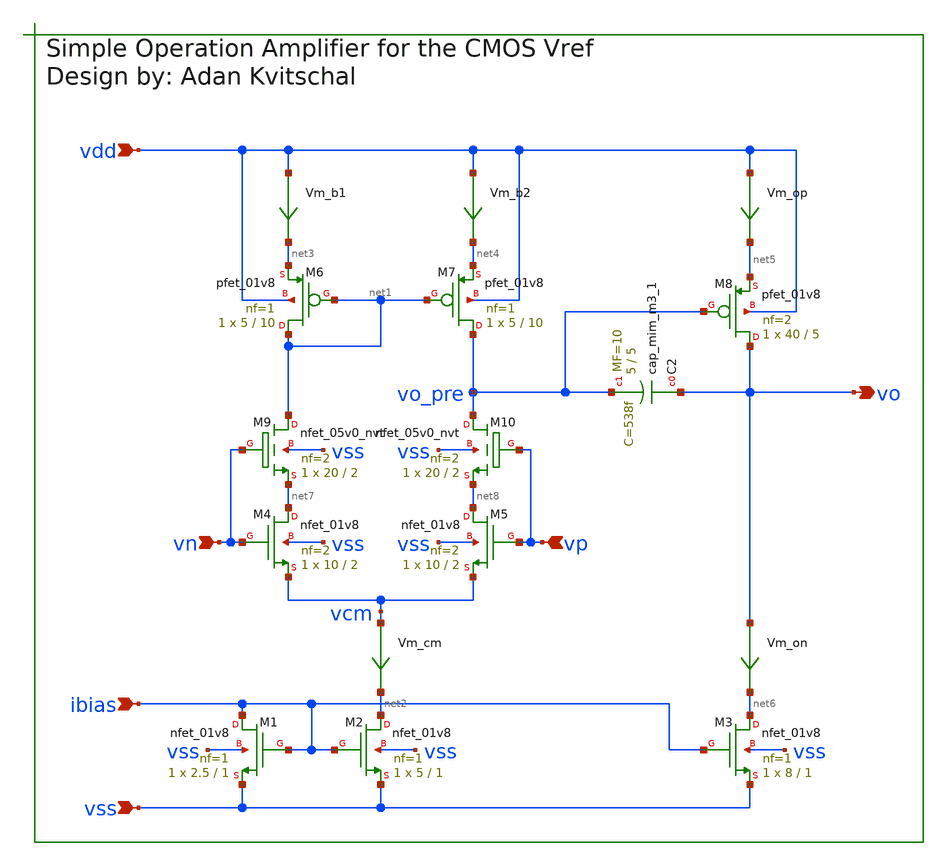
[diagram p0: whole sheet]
** sch_path: xschem/output_amp.sch
**.subckt output_amp vp vn ibias vo vss vdd
*.ipin vp
*.ipin vn
*.ipin ibias
*.opin vo
*.ipin vss
*.ipin vdd
XM1 ibias ibias vss vss sky130_fd_pr__nfet_01v8 L=1 W=2.5 nf=1 ad='int((nf+1)/2) * W/nf * 0.29' as='int((nf+2)/2) * W/nf * 0.29'
+ pd='2*int((nf+1)/2) * (W/nf + 0.29)' ps='2*int((nf+2)/2) * (W/nf + 0.29)' nrd='0.29 / W' nrs='0.29 / W'
+ sa=0 sb=0 sd=0 mult=1 m=1
XM2 net2 ibias vss vss sky130_fd_pr__nfet_01v8 L=1 W=5 nf=1 ad='int((nf+1)/2) * W/nf * 0.29' as='int((nf+2)/2) * W/nf * 0.29'
+ pd='2*int((nf+1)/2) * (W/nf + 0.29)' ps='2*int((nf+2)/2) * (W/nf + 0.29)' nrd='0.29 / W' nrs='0.29 / W'
+ sa=0 sb=0 sd=0 mult=1 m=1
XM7 vo_pre net1 net4 vdd sky130_fd_pr__pfet_01v8 L=10 W=5 nf=1 ad='int((nf+1)/2) * W/nf * 0.29' as='int((nf+2)/2) * W/nf * 0.29'
+ pd='2*int((nf+1)/2) * (W/nf + 0.29)' ps='2*int((nf+2)/2) * (W/nf + 0.29)' nrd='0.29 / W' nrs='0.29 / W'
+ sa=0 sb=0 sd=0 mult=1 m=1
XM4 net7 vn vcm vss sky130_fd_pr__nfet_01v8 L=2 W=10 nf=2 ad='int((nf+1)/2) * W/nf * 0.29' as='int((nf+2)/2) * W/nf * 0.29'
+ pd='2*int((nf+1)/2) * (W/nf + 0.29)' ps='2*int((nf+2)/2) * (W/nf + 0.29)' nrd='0.29 / W' nrs='0.29 / W'
+ sa=0 sb=0 sd=0 mult=1 m=1
XM5 net8 vp vcm vss sky130_fd_pr__nfet_01v8 L=2 W=10 nf=2 ad='int((nf+1)/2) * W/nf * 0.29' as='int((nf+2)/2) * W/nf * 0.29'
+ pd='2*int((nf+1)/2) * (W/nf + 0.29)' ps='2*int((nf+2)/2) * (W/nf + 0.29)' nrd='0.29 / W' nrs='0.29 / W'
+ sa=0 sb=0 sd=0 mult=1 m=1
XM6 net1 net1 net3 vdd sky130_fd_pr__pfet_01v8 L=10 W=5 nf=1 ad='int((nf+1)/2) * W/nf * 0.29' as='int((nf+2)/2) * W/nf * 0.29'
+ pd='2*int((nf+1)/2) * (W/nf + 0.29)' ps='2*int((nf+2)/2) * (W/nf + 0.29)' nrd='0.29 / W' nrs='0.29 / W'
+ sa=0 sb=0 sd=0 mult=1 m=1
Vm_b1 vdd net3 0
.save i(vm_b1)
XM3 net6 ibias vss vss sky130_fd_pr__nfet_01v8 L=1 W=8 nf=1 ad='int((nf+1)/2) * W/nf * 0.29' as='int((nf+2)/2) * W/nf * 0.29'
+ pd='2*int((nf+1)/2) * (W/nf + 0.29)' ps='2*int((nf+2)/2) * (W/nf + 0.29)' nrd='0.29 / W' nrs='0.29 / W'
+ sa=0 sb=0 sd=0 mult=1 m=1
XM8 vo vo_pre net5 vdd sky130_fd_pr__pfet_01v8 L=5 W=40 nf=2 ad='int((nf+1)/2) * W/nf * 0.29' as='int((nf+2)/2) * W/nf * 0.29'
+ pd='2*int((nf+1)/2) * (W/nf + 0.29)' ps='2*int((nf+2)/2) * (W/nf + 0.29)' nrd='0.29 / W' nrs='0.29 / W'
+ sa=0 sb=0 sd=0 mult=1 m=1
Vm_op vdd net5 0
.save i(vm_op)
Vm_cm vcm net2 0
.save i(vm_cm)
Vm_b2 vdd net4 0
.save i(vm_b2)
XC2 vo vo_pre sky130_fd_pr__cap_mim_m3_1 W=5 L=5 MF=10 m=10
Vm_on vo net6 0
.save i(vm_on)
XM9 net1 vn net7 vss sky130_fd_pr__nfet_05v0_nvt L=2 W=20 nf=2 ad='int((nf+1)/2) * W/nf * 0.29' as='int((nf+2)/2) * W/nf * 0.29'
+ pd='2*int((nf+1)/2) * (W/nf + 0.29)' ps='2*int((nf+2)/2) * (W/nf + 0.29)' nrd='0.29 / W' nrs='0.29 / W'
+ sa=0 sb=0 sd=0 mult=1 m=1
XM10 vo_pre vp net8 vss sky130_fd_pr__nfet_05v0_nvt L=2 W=20 nf=2 ad='int((nf+1)/2) * W/nf * 0.29' as='int((nf+2)/2) * W/nf * 0.29'
+ pd='2*int((nf+1)/2) * (W/nf + 0.29)' ps='2*int((nf+2)/2) * (W/nf + 0.29)' nrd='0.29 / W' nrs='0.29 / W'
+ sa=0 sb=0 sd=0 mult=1 m=1
**.ends
.end
